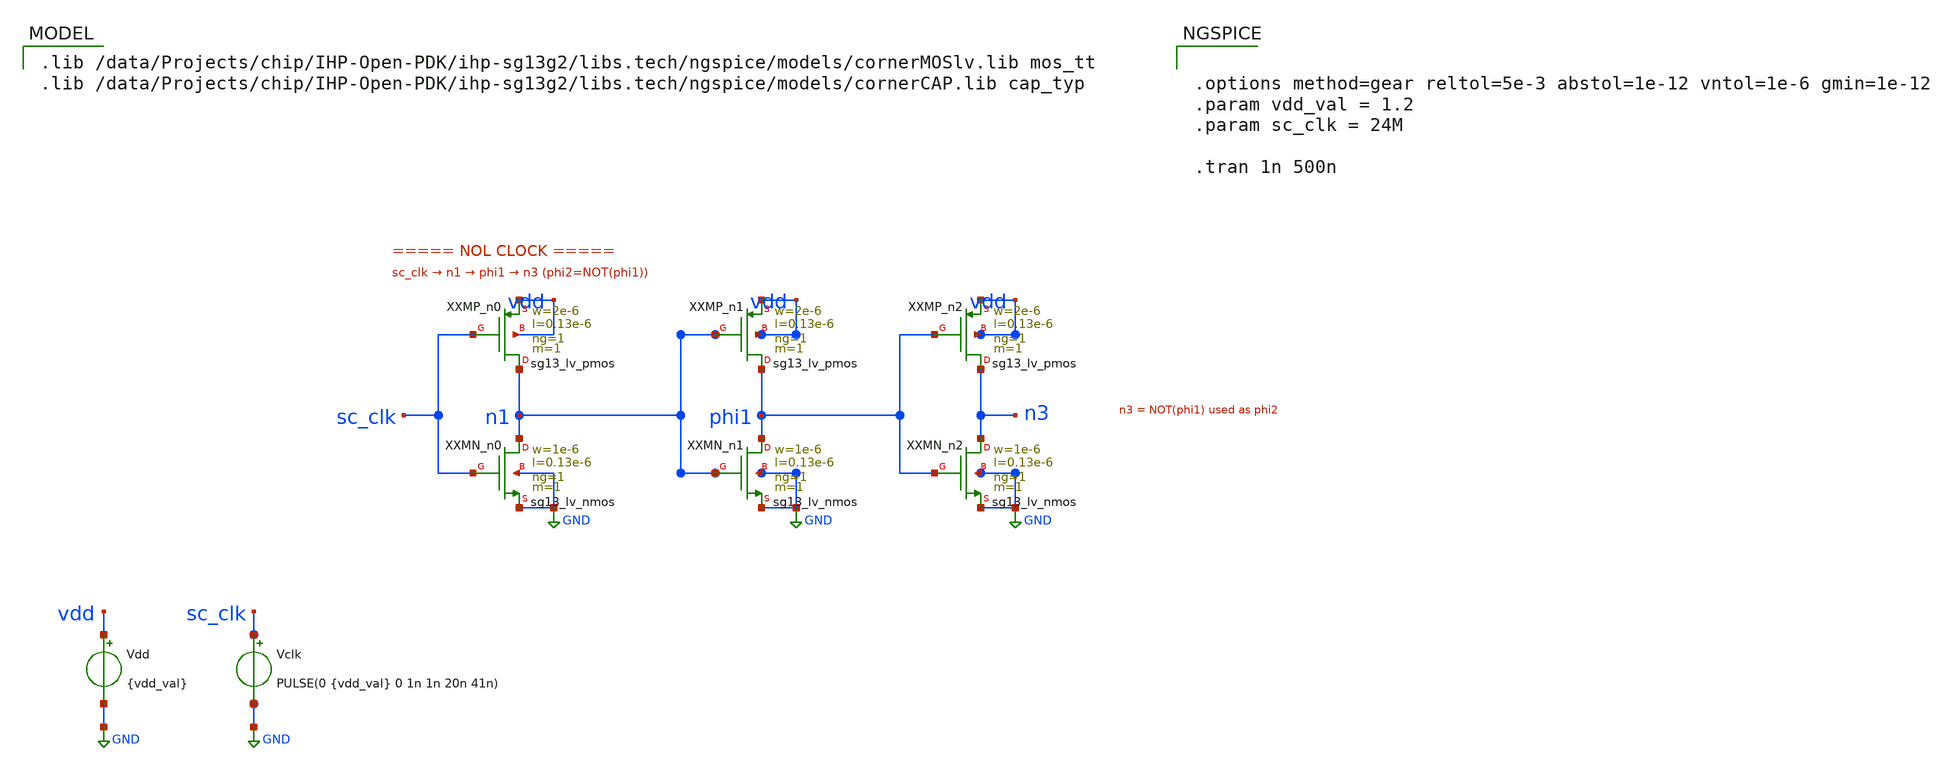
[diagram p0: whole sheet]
** sch_path: xschem/NOL_clk.sch
**.subckt NOL_clk
XXXMP_n0 n1 sc_clk vdd vdd sg13_lv_pmos w=2e-6 l=0.13e-6 ng=1 m=1 mm_ok=1
XXXMN_n0 n1 sc_clk GND GND sg13_lv_nmos w=1e-6 l=0.13e-6 ng=1 m=1 mm_ok=1
XXXMP_n1 phi1 n1 vdd vdd sg13_lv_pmos w=2e-6 l=0.13e-6 ng=1 m=1 mm_ok=1
XXXMN_n1 phi1 n1 GND GND sg13_lv_nmos w=1e-6 l=0.13e-6 ng=1 m=1 mm_ok=1
XXXMP_n2 n3 phi1 vdd vdd sg13_lv_pmos w=2e-6 l=0.13e-6 ng=1 m=1 mm_ok=1
XXXMN_n2 n3 phi1 GND GND sg13_lv_nmos w=1e-6 l=0.13e-6 ng=1 m=1 mm_ok=1
Vclk sc_clk GND PULSE(0 {vdd_val} 0 1n 1n 20n 41n)
Vdd vdd GND {vdd_val}
**** begin user architecture code
 .lib /data/Projects/chip/IHP-Open-PDK/ihp-sg13g2/libs.tech/ngspice/models/cornerMOSlv.lib mos_tt
.lib /data/Projects/chip/IHP-Open-PDK/ihp-sg13g2/libs.tech/ngspice/models/cornerCAP.lib cap_typ



.options method=gear reltol=5e-3 abstol=1e-12 vntol=1e-6 gmin=1e-12
.param vdd_val = 1.2
.param sc_clk = 24M

.tran 1n 500n


**** end user architecture code
**.ends
.GLOBAL GND
.end
